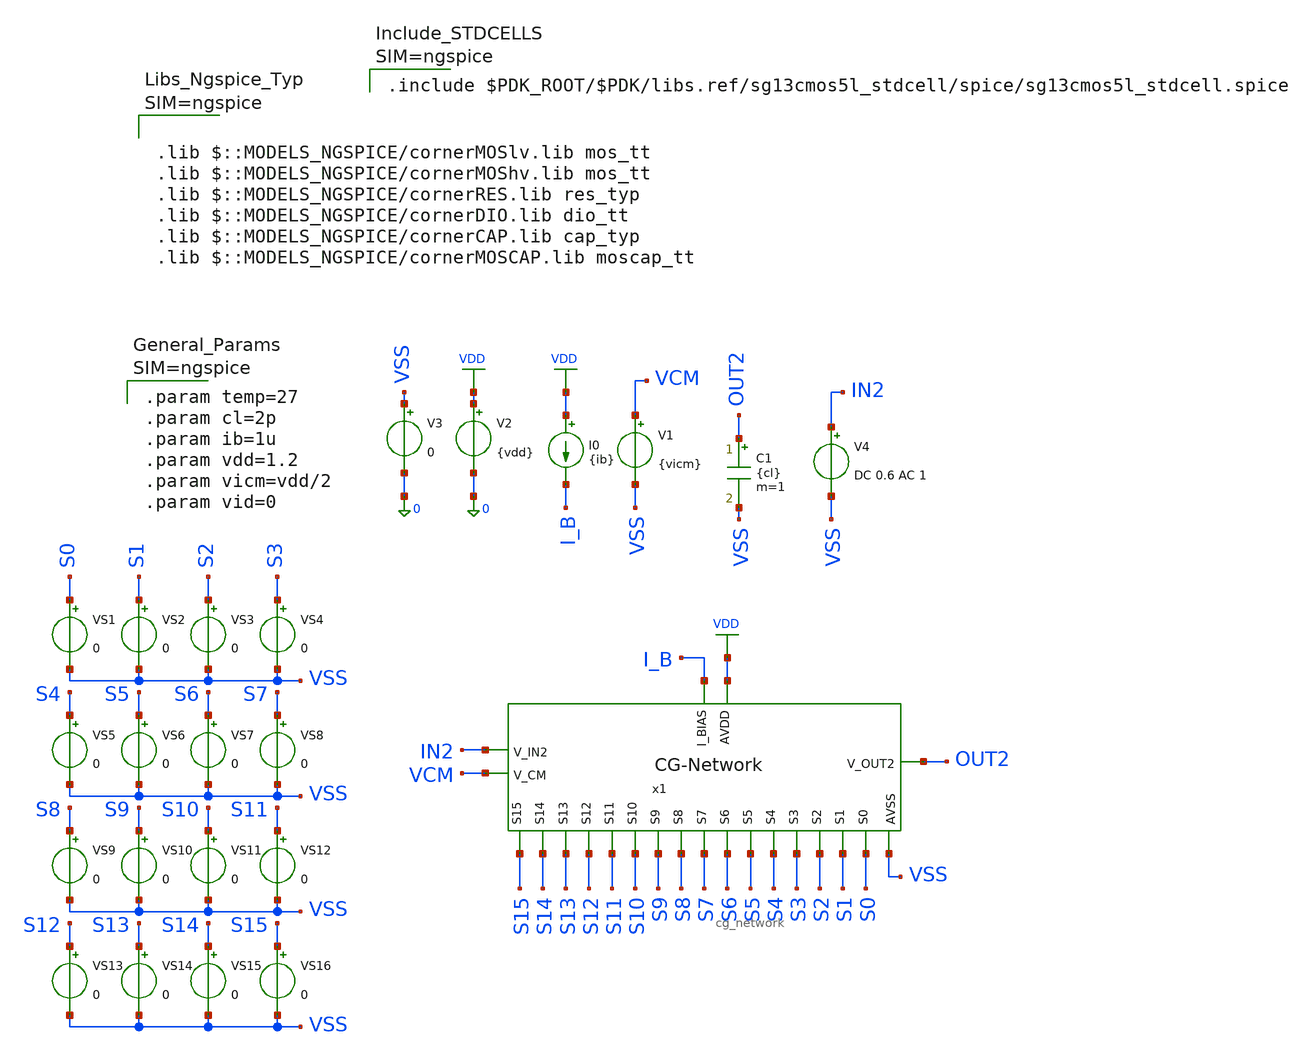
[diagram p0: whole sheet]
** sch_path: xschem/coarse_gain/tb/tb_cg_network/tb_cg_network.sch
**.subckt tb_cg_network
x1 S4 S5 S0 S2 S1 S3 S14 S13 S12 S11 S10 S9 S8 S7 S6 S15 VDD VCM IN2 OUT2 I_B VSS cg_network
I0 VDD I_B {ib}
V2 VDD 0 {vdd}
V3 VSS 0 0
V1 VCM VSS {vicm}
C1 OUT2 VSS {cl} m=1
VS1 S0 VSS 0
VS2 S1 VSS 0
VS3 S2 VSS 0
VS4 S3 VSS 0
VS5 S4 VSS 0
VS6 S5 VSS 0
VS7 S6 VSS 0
VS8 S7 VSS 0
VS9 S8 VSS 0
VS10 S9 VSS 0
VS11 S10 VSS 0
VS12 S11 VSS 0
VS13 S12 VSS 0
VS14 S13 VSS 0
VS15 S14 VSS 0
VS16 S15 VSS 0
V4 IN2 VSS DC 0.6 AC 1
**** begin user architecture code


.param temp=27
.param cl=2p
.param ib=1u
.param vdd=1.2
.param vicm=vdd/2
.param vid=0






.lib $::MODELS_NGSPICE/cornerMOSlv.lib mos_tt
.lib $::MODELS_NGSPICE/cornerMOShv.lib mos_tt
.lib $::MODELS_NGSPICE/cornerRES.lib res_typ
.lib $::MODELS_NGSPICE/cornerDIO.lib dio_tt
.lib $::MODELS_NGSPICE/cornerCAP.lib cap_typ
.lib $::MODELS_NGSPICE/cornerMOSCAP.lib moscap_tt





.control
* ==============================================================================
* COARSE-GAIN NETWORK (PGA) 16-TAP AUTOMATED TELEMETRY & ACCURACY CHARACTERIZATION
* Topology  : Inverting Closed-Loop Logarithmic Resistor Ladder (R to 649R)
* Technology: IHP SG13CMOS5L (130nm BiCMOS)
* ==============================================================================

destroy all
save all
shell mkdir -p result
shell rm -f ./result/tb_cg_network_summary.txt

echo
+ "==================================================================================================================================================" >> ./result/tb_cg_network_summary.txt
echo " Tap   Code   Target(dB)   Meas(dB)   Err(dB)    Err(Step)   Acc_FS(%)    -3dB BW(Hz)
+    Vos_out(mV)   V_vg_err(mV)   P_dc(uW) " >> ./result/tb_cg_network_summary.txt
echo
+ "==================================================================================================================================================" >> ./result/tb_cg_network_summary.txt

echo
+ "=================================================================================================================================================="
echo " STARTING AUTOMATED 16-TAP PGA AC & DC TELEMETRY CHARACTERIZATION (DB-BASED ERROR)
+                                                                "
echo
+ "=================================================================================================================================================="

* ------------------------------------------------------------------------------
* STEP 0: DC OFFSET PRE-CALIBRATION
* ------------------------------------------------------------------------------
alter @vs1[dc]  = 1.2
alter @vs2[dc]  = 0
alter @vs3[dc]  = 0
alter @vs4[dc]  = 0
alter @vs5[dc]  = 0
alter @vs6[dc]  = 0
alter @vs7[dc]  = 0
alter @vs8[dc]  = 0
alter @vs9[dc]  = 0
alter @vs10[dc] = 0
alter @vs11[dc] = 0
alter @vs12[dc] = 0
alter @vs13[dc] = 0
alter @vs14[dc] = 0
alter @vs15[dc] = 0
alter @vs16[dc] = 0

op
let v_vg_nominal = v(x1.net17)
echo " Calibrated Input DC Bias to Virtual Ground: " $&v_vg_nominal " V"

alter @v4[dc] = $&v_vg_nominal

set appendwrite

* ------------------------------------------------------------------------------
* STEP 1: SEQUENTIAL 16-TAP EVALUATION LOOP
* ------------------------------------------------------------------------------
foreach tap 0 1 2 3 4 5 6 7 8 9 10 11 12 13 14 15

  * Reset all switch voltages
  alter @vs1[dc]  = 0
  alter @vs2[dc]  = 0
  alter @vs3[dc]  = 0
  alter @vs4[dc]  = 0
  alter @vs5[dc]  = 0
  alter @vs6[dc]  = 0
  alter @vs7[dc]  = 0
  alter @vs8[dc]  = 0
  alter @vs9[dc]  = 0
  alter @vs10[dc] = 0
  alter @vs11[dc] = 0
  alter @vs12[dc] = 0
  alter @vs13[dc] = 0
  alter @vs14[dc] = 0
  alter @vs15[dc] = 0
  alter @vs16[dc] = 0

  * Assert active tap
  if ($tap = 0)
    alter @vs1[dc] = 1.2
  end
  if ($tap = 1)
    alter @vs2[dc] = 1.2
  end
  if ($tap = 2)
    alter @vs3[dc] = 1.2
  end
  if ($tap = 3)
    alter @vs4[dc] = 1.2
  end
  if ($tap = 4)
    alter @vs5[dc] = 1.2
  end
  if ($tap = 5)
    alter @vs6[dc] = 1.2
  end
  if ($tap = 6)
    alter @vs7[dc] = 1.2
  end
  if ($tap = 7)
    alter @vs8[dc] = 1.2
  end
  if ($tap = 8)
    alter @vs9[dc] = 1.2
  end
  if ($tap = 9)
    alter @vs10[dc] = 1.2
  end
  if ($tap = 10)
    alter @vs11[dc] = 1.2
  end
  if ($tap = 11)
    alter @vs12[dc] = 1.2
  end
  if ($tap = 12)
    alter @vs13[dc] = 1.2
  end
  if ($tap = 13)
    alter @vs14[dc] = 1.2
  end
  if ($tap = 14)
    alter @vs15[dc] = 1.2
  end
  if ($tap = 15)
    alter @vs16[dc] = 1.2
  end

  * Run DC Operating Point
  op
  let cur_vos_mv  = (v(out2) - v(vcm)) * 1e3
  let cur_vvg_mv  = (v(x1.net17) - v(vcm)) * 1e3
  let cur_pdc_uw  = -i(v2) * 1.2 * 1e6

  set s_vos = "$&cur_vos_mv"
  set s_vvg = "$&cur_vvg_mv"
  set s_pdc = "$&cur_pdc_uw"

  * Run AC Analysis
  ac dec 30 10 100MEG

  let gain_db = db(v(out2))
  let ph_deg  = cph(v(out2)) * 180 / pi

  * Measure midband gain at 1 kHz flatband
  meas ac g_meas_db find gain_db at=1k

  * Measure -3 dB bandwidth
  let target_3db = g_meas_db - 3
  meas ac f_3db when gain_db=target_3db

  * Calculate theoretical gain and dB-based error metrics
  let ideal_db   = $tap * 3.75
  let err_db     = g_meas_db - ideal_db
  let err_step   = err_db / 3.75
  let acc_fs     = 100 - (abs(err_db) / 56.25 * 100)

  write ./result/tb_cg_network_all_taps.raw gain_db ph_deg

  * Telemetry Output
  echo " S$tap | Target: $&ideal_db dB | Meas: $&g_meas_db dB | Err: $&err_db dB ($&err_step Step) |
+ Acc_FS: $&acc_fs % | -3dB BW: $&f_3db Hz | Vos: $s_vos mV"

  echo " S$tap  |  $tap  |  $&ideal_db  |  $&g_meas_db  |  $&err_db  |  $&err_step  |  $&acc_fs  |
+  $&f_3db  |  $s_vos  |  $s_vvg  |  $s_pdc" >> ./result/tb_cg_network_summary.txt

end

unset appendwrite
echo
+ "=================================================================================================================================================="
echo " CHARACTERIZATION COMPLETED! Full telemetry log is exported to:
+                                                                                   "
echo " ./result/tb_cg_network_summary.txt
+                                                                                                              "
echo
+ "=================================================================================================================================================="
.endc




.include $PDK_ROOT/$PDK/libs.ref/sg13cmos5l_stdcell/spice/sg13cmos5l_stdcell.spice



**** end user architecture code
**.ends

* expanding   symbol:
*+  /foss/designs/Programmable-Instrumentation-Amplifier-IP/designs/libs/core_analog/coarse_gain/cg_network.sym # of pins=22
** sym_path: xschem/coarse_gain/cg_network.sym
** sch_path: xschem/coarse_gain/cg_network.sch
.subckt cg_network S4 S5 S0 S2 S1 S3 S14 S13 S12 S11 S10 S9 S8 S7 S6 S15 AVDD V_CM V_IN2 V_OUT2
+ I_BIAS AVSS
*.ipin I_BIAS
*.ipin V_IN2
*.ipin V_CM
*.ipin AVSS
*.ipin AVDD
*.opin V_OUT2
*.ipin S15
*.ipin S14
*.ipin S13
*.ipin S12
*.ipin S11
*.ipin S10
*.ipin S9
*.ipin S8
*.ipin S7
*.ipin S6
*.ipin S5
*.ipin S4
*.ipin S3
*.ipin S2
*.ipin S1
*.ipin S0
x1 AVDD V_CM net17 V_OUT2 I_BIAS AVSS cg_ota
XR2 net12 net13 AVSS rhigh w=0.5e-6 l=9.6e-6 m=1 b=32 mm_ok=1
XR3 net13 net14 AVSS rhigh w=0.5e-6 l=4.5e-6 m=1 b=32 mm_ok=1
XR4 net14 net15 AVSS rhigh w=0.5e-6 l=5e-6 m=1 b=16 mm_ok=1
XR5 net15 net16 AVSS rhigh w=0.5e-6 l=5.5e-6 m=1 b=8 mm_ok=1
XR6 net16 net11 AVSS rhigh w=0.5e-6 l=4.7e-6 m=1 b=4 mm_ok=1
XR7 net11 net10 AVSS rhigh w=0.5e-6 l=5.41e-6 m=1 b=2 mm_ok=1
XR8 net10 net9 AVSS rhigh w=0.5e-6 l=3.34e-6 m=1 b=2 mm_ok=1
XR9 net9 net8 AVSS rhigh w=0.5e-6 l=7.39e-6 m=1 b=0 mm_ok=1
XR10 net8 net7 AVSS rhigh w=0.5e-6 l=4.76e-6 m=1 b=0 mm_ok=1
XR11 net7 net6 AVSS rhigh w=0.5e-6 l=3.06e-6 m=1 b=0 mm_ok=1
XR12 net6 net5 AVSS rhigh w=0.5e-6 l=1.94e-6 m=1 b=0 mm_ok=1
XR16 net2 net1 AVSS rppd w=2e-6 l=8.08e-6 m=1 b=0 mm_ok=1
XR17 net3 net2 AVSS rppd w=2e-6 l=5.1e-6 m=1 b=1 mm_ok=1
XR15 net1 V_OUT2 AVSS rppd w=2e-6 l=7.6e-6 m=1 b=0 mm_ok=1
XR18 net17 V_IN2 AVSS rppd w=0.5e-6 l=3.62e-6 m=1 b=0 mm_ok=1
XR1 net4 net3 AVSS rppd w=2e-6 l=8.65e-6 m=1 b=1 mm_ok=1
XR13 net5 net4 AVSS rppd w=2e-6 l=8.5e-6 m=1 b=2 mm_ok=1
x18 net18 S15 AVDD AVSS sg13cmos5l_inv_1
x19 net19 S14 AVDD AVSS sg13cmos5l_inv_1
x20 net20 S13 AVDD AVSS sg13cmos5l_inv_1
x21 net21 S12 AVDD AVSS sg13cmos5l_inv_1
x22 net22 S11 AVDD AVSS sg13cmos5l_inv_1
x23 net23 S10 AVDD AVSS sg13cmos5l_inv_1
x24 net24 S9 AVDD AVSS sg13cmos5l_inv_1
x25 net25 S8 AVDD AVSS sg13cmos5l_inv_1
x26 net26 S7 AVDD AVSS sg13cmos5l_inv_1
x27 net27 S6 AVDD AVSS sg13cmos5l_inv_1
x28 net28 S5 AVDD AVSS sg13cmos5l_inv_1
x29 net29 S4 AVDD AVSS sg13cmos5l_inv_1
x30 net30 S3 AVDD AVSS sg13cmos5l_inv_1
x31 net31 S2 AVDD AVSS sg13cmos5l_inv_1
x32 net32 S1 AVDD AVSS sg13cmos5l_inv_1
x33 net33 S0 AVDD AVSS sg13cmos5l_inv_1
x2 net17 AVSS AVDD S15 net18 net12 tgate
x3 net17 AVSS AVDD S14 net19 net13 tgate
x4 net17 AVSS AVDD S13 net20 net14 tgate
x5 net17 AVSS AVDD S12 net21 net15 tgate
x6 net17 AVSS AVDD S11 net22 net16 tgate
x7 net17 AVSS AVDD S10 net23 net11 tgate
x8 net17 AVSS AVDD S9 net24 net10 tgate
x9 net17 AVSS AVDD S8 net25 net9 tgate
x10 net17 AVSS AVDD S7 net26 net8 tgate
x11 net17 AVSS AVDD S6 net27 net7 tgate
x12 net17 AVSS AVDD S5 net28 net6 tgate
x13 net17 AVSS AVDD S4 net29 net5 tgate
x14 net17 AVSS AVDD S3 net30 net4 tgate
x15 net17 AVSS AVDD S2 net31 net3 tgate
x16 net17 AVSS AVDD S1 net32 net2 tgate
x17 net17 AVSS AVDD S0 net33 net1 tgate
.ends


* expanding   symbol:
*+  /foss/designs/Programmable-Instrumentation-Amplifier-IP/designs/libs/core_analog/coarse_gain/cg_ota.sym # of pins=6
** sym_path: designs/libs/core_analog/coarse_gain/cg_ota.sym
** sch_path: designs/libs/core_analog/coarse_gain/cg_ota.sch
.subckt cg_ota VDD V_inp V_inn V_out I_bias VSS
*.ipin V_inn
*.ipin VDD
*.ipin VSS
*.opin V_out
*.ipin I_bias
*.ipin V_inp
XM1 F1 V_inn net6 VDD sg13_lv_pmos w=26.56u l=2u ng=4 m=1 mm_ok=1
XM2 F2 V_inp net6 VDD sg13_lv_pmos w=26.56u l=2u ng=4 m=1 mm_ok=1
XM3 net5 net5 VDD VDD sg13_lv_pmos w=7.33u l=2u ng=1 m=1 mm_ok=1
XM4 N_A net5 VDD VDD sg13_lv_pmos w=7.33u l=2u ng=1 m=1 mm_ok=1
XM7 F1 V_bn2 VSS VSS sg13_lv_nmos w=9.21u l=2u ng=1 m=1 mm_ok=1
XM8 F2 V_bn2 VSS VSS sg13_lv_nmos w=9.21u l=2u ng=1 m=1 mm_ok=1
XM_tail net6 V_btail VDD VDD sg13_lv_pmos w=7.46u l=2u ng=1 m=8 mm_ok=1
XM_ctrlp N_B V_ctrlp N_A VDD sg13_lv_pmos w=2.20u l=0.50u ng=1 m=1 mm_ok=1
XM_outp V_out N_A VDD VDD sg13_lv_pmos w=22.20u l=0.5u ng=4 m=1 mm_ok=1
XM_ctrln N_A V_ctrln N_B VSS sg13_lv_nmos w=0.84u l=0.5u ng=1 m=1 mm_ok=1
XM_outn V_out N_B VSS VSS sg13_lv_nmos w=8.4u l=0.5u ng=1 m=1 mm_ok=1
XM5 net5 V_bn1 F1 VSS sg13_lv_nmos w=6.41u l=2u ng=1 m=1 mm_ok=1
XM6 N_A V_bn1 F2 VSS sg13_lv_nmos w=6.41u l=2u ng=1 m=1 mm_ok=1
XM_mp1 net1 net1 VDD VDD sg13_lv_pmos w=2.30u l=2u ng=1 m=1 mm_ok=1
XM_mn1 net1 I_bias VSS VSS sg13_lv_nmos w=0.87u l=2u ng=1 m=1 mm_ok=1
XM_refn I_bias I_bias VSS VSS sg13_lv_nmos w=0.87u l=2u ng=1 m=1 mm_ok=1
XM_mp2 V_bn1 net1 VDD VDD sg13_lv_pmos w=11.50u l=2u ng=2 m=1 mm_ok=1
XM_mp3 V_bn2 net1 VDD VDD sg13_lv_pmos w=23u l=2u ng=4 m=1 mm_ok=1
XM_bn1 V_bn1 V_bn1 net2 VSS sg13_lv_nmos w=1.60u l=2u ng=1 m=1 mm_ok=1
XM_bn2 V_bn2 V_bn2 VSS VSS sg13_lv_nmos w=9.21u l=2u ng=1 m=1 mm_ok=1
XM_mn2 V_btail I_bias VSS VSS sg13_lv_nmos w=6u l=2u ng=1 m=1 mm_ok=1
XM_rep_tail V_btail V_btail VDD VDD sg13_lv_pmos w=7.46u l=2u ng=1 m=8 mm_ok=1
XM_mn4 N_B I_bias VSS VSS sg13_lv_nmos w=3.48u l=2u ng=1 m=1 mm_ok=1
XC1 F2 V_out cap_cmomf w=26.48e-6 l=26.48e-6 mmin=1 mmax=4 subblock=0 rfmodel=0 subscale=1 m=1
+ mm_ok=1
XC2 N_A V_out cap_cmomf w=22.07e-6 l=22.07e-6 mmin=1 mmax=4 subblock=0 rfmodel=0 subscale=1 m=1
+ mm_ok=1
XR1 net2 VSS VSS rhigh w=0.5e-6 l=17e-6 m=1 b=0 mm_ok=1
XM_mp4 V_ctrln net1 VDD VDD sg13_lv_pmos w=4.60u l=2u ng=1 m=1 mm_ok=1
XM_rep_ctrln V_ctrln V_ctrln net3 VSS sg13_lv_nmos w=0.84u l=0.5u ng=1 m=1 mm_ok=1
XM_rep_outn net3 net3 VSS VSS sg13_lv_nmos w=2.10u l=0.5u ng=1 m=1 mm_ok=1
XM_mn3 V_ctrlp I_bias VSS VSS sg13_lv_nmos w=1.74u l=2u ng=1 m=1 mm_ok=1
XM_rep_outp net4 net4 VDD VDD sg13_lv_pmos w=5.55u l=0.5u ng=1 m=1 mm_ok=1
XM_rep_ctrlp V_ctrlp V_ctrlp net4 VDD sg13_lv_pmos w=2.20u l=0.50u ng=1 m=1 mm_ok=1
XM_mp5 N_A net1 VDD VDD sg13_lv_pmos w=9.2u l=2u ng=1 m=1 mm_ok=1
.ends


* expanding   symbol:
*+  /foss/designs/Programmable-Instrumentation-Amplifier-IP/designs/libs/core_digital/tgate/tgate.sym # of pins=6
** sym_path: designs/libs/core_digital/tgate/tgate.sym
** sch_path: designs/libs/core_digital/tgate/tgate.sch
.subckt tgate IN AVSS AVDD EN ENB OUT
*.iopin AVDD
*.iopin AVSS
*.iopin IN
*.iopin OUT
*.ipin EN
*.ipin ENB
XM1 IN EN OUT AVSS sg13_lv_nmos w=1u l=0.13u ng=1 m=1 mm_ok=1
XM2 OUT ENB IN AVDD sg13_lv_pmos w=2.5u l=0.13u ng=1 m=1 mm_ok=1
.ends

.GLOBAL VDD
.end
